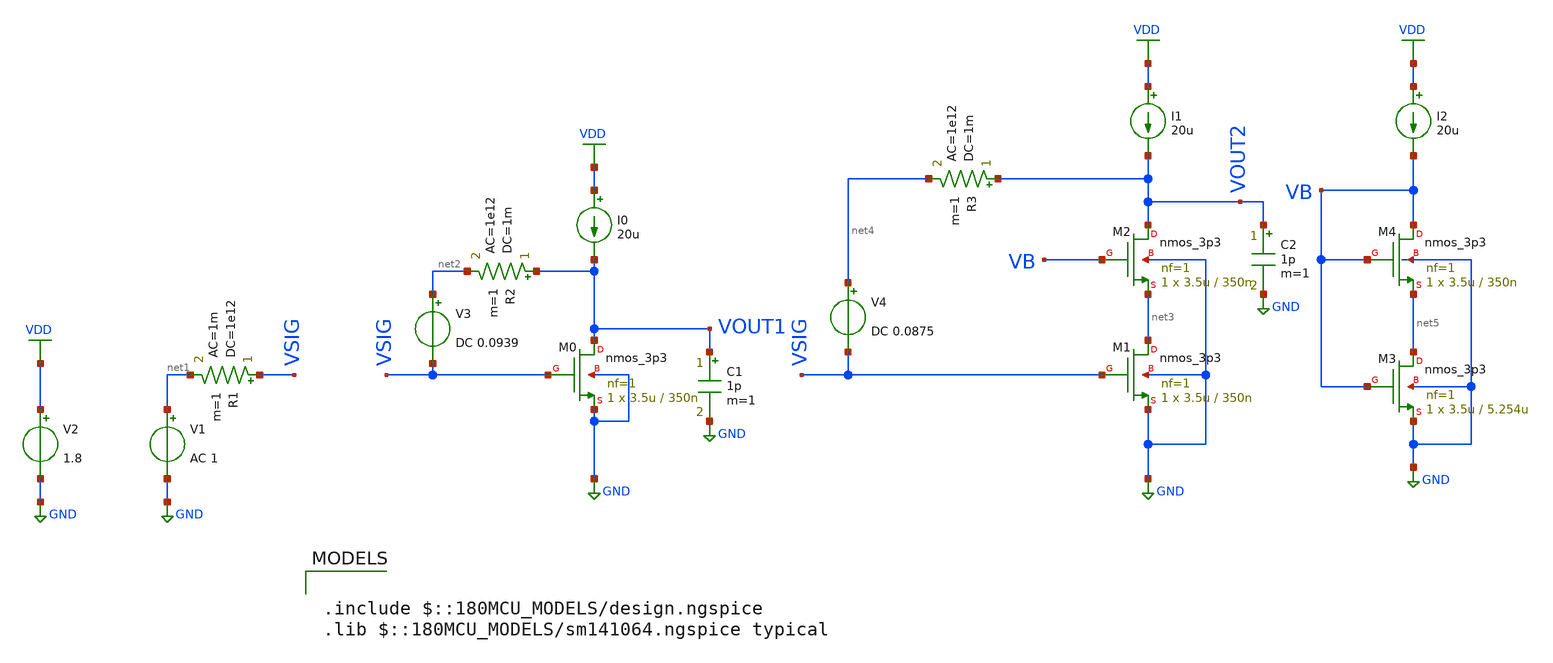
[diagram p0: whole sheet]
** sch_path: ITI_Labs/Lab3/Design/Lab03.sch
**.subckt Lab03
V1 net1 GND AC 1
R1 VSIG net1 1e12 ac=1m m=1
XM0 VOUT1 VSIG GND GND nmos_3p3 L=350n W=3.5u nf=1 ad='int((nf+1)/2) * W/nf * 0.18u' as='int((nf+2)/2) * W/nf * 0.18u'
+ pd='2*int((nf+1)/2) * (W/nf + 0.18u)' ps='2*int((nf+2)/2) * (W/nf + 0.18u)' nrd='0.18u / W' nrs='0.18u / W'
+ sa=0 sb=0 sd=0 m=1
I0 VDD VOUT1 20u
C1 VOUT1 GND 1p m=1
V2 VDD GND 1.8
V3 net2 VSIG DC 0.0939
R2 VOUT1 net2 1m ac=1e12 m=1
XM1 net3 VSIG GND GND nmos_3p3 L=350n W=3.5u nf=1 ad='int((nf+1)/2) * W/nf * 0.18u' as='int((nf+2)/2) * W/nf * 0.18u'
+ pd='2*int((nf+1)/2) * (W/nf + 0.18u)' ps='2*int((nf+2)/2) * (W/nf + 0.18u)' nrd='0.18u / W' nrs='0.18u / W'
+ sa=0 sb=0 sd=0 m=1
XM2 VOUT2 VB net3 GND nmos_3p3 L=350n W=3.5u nf=1 ad='int((nf+1)/2) * W/nf * 0.18u' as='int((nf+2)/2) * W/nf * 0.18u'
+ pd='2*int((nf+1)/2) * (W/nf + 0.18u)' ps='2*int((nf+2)/2) * (W/nf + 0.18u)' nrd='0.18u / W' nrs='0.18u / W'
+ sa=0 sb=0 sd=0 m=1
V4 net4 VSIG DC 0.0875
I1 VDD VOUT2 20u
R3 VOUT2 net4 1m ac=1e12 m=1
C2 VOUT2 GND 1p m=1
XM4 VB VB net5 GND nmos_3p3 L=350n W=3.5u nf=1 ad='int((nf+1)/2) * W/nf * 0.18u' as='int((nf+2)/2) * W/nf * 0.18u'
+ pd='2*int((nf+1)/2) * (W/nf + 0.18u)' ps='2*int((nf+2)/2) * (W/nf + 0.18u)' nrd='0.18u / W' nrs='0.18u / W'
+ sa=0 sb=0 sd=0 m=1
I2 VDD VB 20u
XM3 net5 VB GND GND nmos_3p3 L=5.254u W=3.5u nf=1 ad='int((nf+1)/2) * W/nf * 0.18u' as='int((nf+2)/2) * W/nf * 0.18u'
+ pd='2*int((nf+1)/2) * (W/nf + 0.18u)' ps='2*int((nf+2)/2) * (W/nf + 0.18u)' nrd='0.18u / W' nrs='0.18u / W'
+ sa=0 sb=0 sd=0 m=1
**** begin user architecture code

.include $::180MCU_MODELS/design.ngspice
.lib $::180MCU_MODELS/sm141064.ngspice typical



.include sim_script.inc


**** end user architecture code
**.ends
.GLOBAL GND
.GLOBAL VDD
.end
